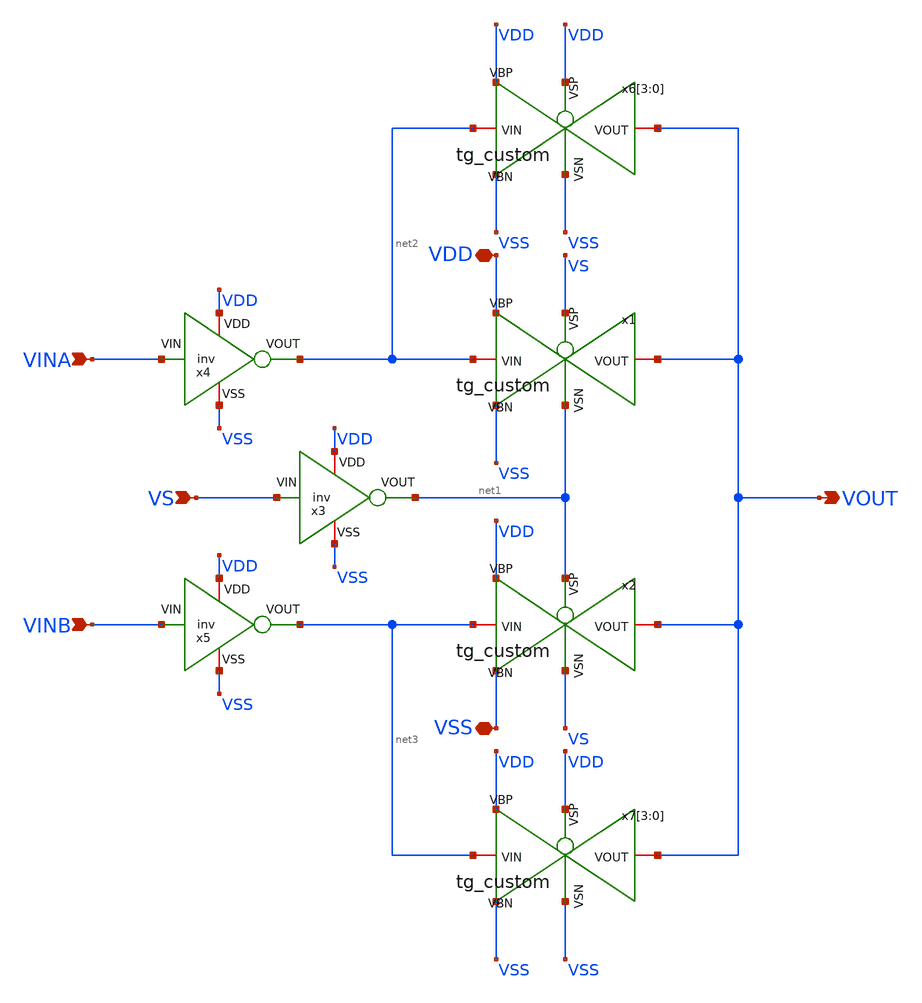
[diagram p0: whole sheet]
** sch_path: Custom_std_cells/MUX_2_1.sch
**.subckt MUX_2_1 VOUT VINA VINB VS VDD VSS
*.opin VOUT
*.ipin VINA
*.ipin VINB
*.ipin VS
*.iopin VDD
*.iopin VSS
x1 VOUT net1 VS net2 VDD VSS tg_custom
x2 VOUT VS net1 net3 VDD VSS tg_custom
x3 VDD net1 VS VSS inv
x4 VDD net2 VINA VSS inv
x5 VDD net3 VINB VSS inv
x6[3] VOUT VSS VDD net2 VDD VSS tg_custom
x6[2] VOUT VSS VDD net2 VDD VSS tg_custom
x6[1] VOUT VSS VDD net2 VDD VSS tg_custom
x6[0] VOUT VSS VDD net2 VDD VSS tg_custom
x7[3] VOUT VSS VDD net3 VDD VSS tg_custom
x7[2] VOUT VSS VDD net3 VDD VSS tg_custom
x7[1] VOUT VSS VDD net3 VDD VSS tg_custom
x7[0] VOUT VSS VDD net3 VDD VSS tg_custom
**.ends

* expanding   symbol:  /foss/designs/PhaseInterpolator/Custom_std_cells/tg_custom.sym # of pins=6
** sym_path: /foss/designs/PhaseInterpolator/Custom_std_cells/tg_custom.sym
** sch_path: /foss/designs/PhaseInterpolator/Custom_std_cells/tg_custom.sch
.subckt tg_custom VOUT VSN VSP VIN VBP VBN
*.iopin VIN
*.iopin VSN
*.iopin VOUT
*.iopin VSP
*.iopin VBN
*.iopin VBP
XM1 VOUT VSN VIN VBN sg13_lv_nmos w=0.15u l=0.13u ng=1 m=1 mm_ok=1
XM2 VOUT VSP VIN VBP sg13_lv_pmos w=0.15u l=0.13u ng=1 m=2 mm_ok=1
.ends

.end
